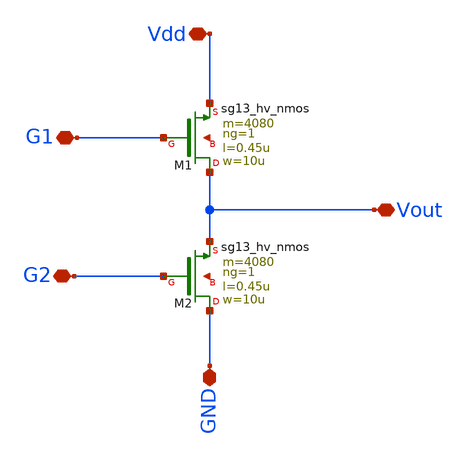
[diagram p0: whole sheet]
** sch_path: Rediseno/2NmosSch.sch
**.subckt 2NmosSch Vout G1 G2 Vdd GND
*.iopin Vout
*.iopin G1
*.iopin G2
*.iopin Vdd
*.iopin GND
XM2 GND G2 Vout net1 sg13_hv_nmos w=10u l=0.45u ng=1 m=4080 mm_ok=1
XM1 Vout G1 Vdd net2 sg13_hv_nmos w=10u l=0.45u ng=1 m=4080 mm_ok=1
**.ends
.end
